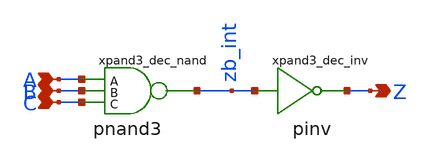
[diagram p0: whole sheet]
** sch_path: sram_2_64_scn4m_lcc/and3_dec.sch
**.subckt and3_dec A B C Z
*.ipin A
*.ipin B
*.ipin C
*.opin Z
xpand3_dec_nand A B C zb_int vdd gnd pnand3
xpand3_dec_inv zb_int Z vdd gnd pinv
**.ends
.end
